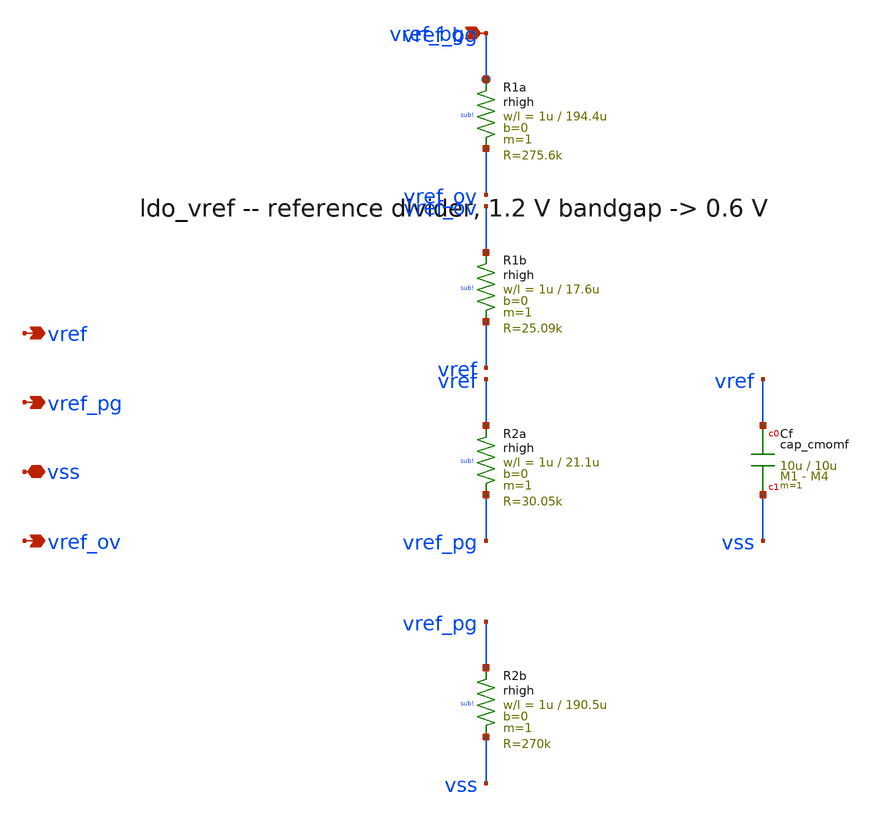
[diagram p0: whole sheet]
** sch_path: xschem/ldo_vref.sch
**.subckt ldo_vref vref_bg vref vref_pg vss vref_ov
*.ipin vref_bg
*.opin vref
*.opin vref_pg
*.iopin vss
*.opin vref_ov
XR1a vref_bg vref_ov sub! rhigh w=1u l=194.4u m=1 b=0 mm_ok=1
XR1b vref_ov vref sub! rhigh w=1u l=17.6u m=1 b=0 mm_ok=1
XR2a vref vref_pg sub! rhigh w=1u l=21.1u m=1 b=0 mm_ok=1
XR2b vref_pg vss sub! rhigh w=1u l=190.5u m=1 b=0 mm_ok=1
XCf vref vss cap_cmomf w=10u l=10u mmin=1 mmax=4 subblock=0 rfmodel=0 subscale=1 m=1 mm_ok=1
**.ends
.end
